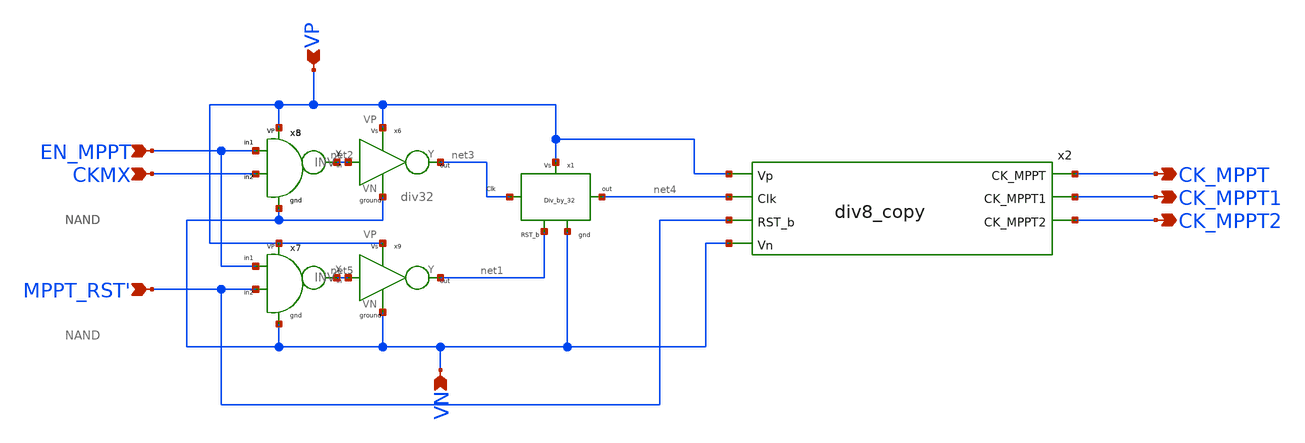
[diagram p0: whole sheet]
** sch_path: Blocks/MPPT/MPPT Clock initial stage.sch
**.subckt MPPT Clock initial stage CKMX MPPT_RST' VP EN_MPPT CK_MPPT CK_MPPT1 CK_MPPT2 VN
*.ipin CKMX
*.ipin MPPT_RST'
*.ipin VP
*.ipin EN_MPPT
*.opin CK_MPPT
*.opin CK_MPPT1
*.opin CK_MPPT2
*.ipin VN
x2 VP net4 CK_MPPT MPPT_RST' VN CK_MPPT1 CK_MPPT2 div8_copy
x1 net3 net4 VP VN net1 div32
x5 CKMX EN_MPPT net2 VP VN NAND
x7 MPPT_RST' EN_MPPT net5 VP VN NAND
x6 net2 net3 VP VN INV
x8 CKMX EN_MPPT net2 VP VN NAND
x9 net5 net1 VP VN INV
**.ends

* expanding   symbol:  Blocks/MPPT/div8_copy.sym # of pins=7
** sym_path: Blocks/MPPT/div8_copy.sym
** sch_path: Blocks/MPPT/div8_copy.sch
.subckt div8_copy Vp Clk CK_MPPT RST_b Vn CK_MPPT1 CK_MPPT2
*.ipin Clk
*.ipin RST_b
*.opin CK_MPPT
*.opin CK_MPPT1
*.opin CK_MPPT2
*.ipin Vn
*.ipin Vp
x1 net2 Clk RST_b Vn Vp net1 net2 DFF1
x2 net3 net1 RST_b Vn Vp net4 net3 DFF1
x3 net6 net4 RST_b Vn Vp net5 net6 DFF1
x4 net7 CK_MPPT Vp Vn INV
x5 net8 CK_MPPT1 Vp Vn INV
x7 net9 CK_MPPT2 Vp Vn INV
x8 net1 net12 Vp Vn INV
x11 net4 net11 Vp Vn INV
x12 net4 net10 Vp Vn INV
x6 net5 net11 net12 Vp Vn net9 NAND3
x9 net5 net10 net1 Vp Vn net8 NAND3
x10 net5 net4 net1 Vp Vn net7 NAND3
.ends


* expanding   symbol:  Blocks/Divide by 32 ckt/div32.sym # of pins=5
** sym_path: Blocks/Divide by 32 ckt/div32.sym
** sch_path: Blocks/Divide by 32 ckt/div32.sch
.subckt div32 Clk Clk/32 VP VN RST_b
*.opin Clk/32
*.ipin Clk
*.iopin VP
*.iopin VN
*.ipin RST_b
x1 net2 Clk RST_b VN VP net1 net2 DFF1
x6 net9 net10 VN VP Buff
x2 net3 net1 RST_b VN VP net4 net3 DFF1
x3 net8 net4 RST_b VN VP net5 net8 DFF1
x4 net7 net5 RST_b VN VP net6 net7 DFF1
x5 net9 net6 RST_b VN VP Clk/32 net10 DFF1
.ends


* expanding   symbol:  component/NAND2/NAND.sym # of pins=5
** sym_path: component/NAND2/NAND.sym
** sch_path: component/NAND2/NAND.sch
.subckt NAND B A Y VP VN
*.iopin VP
*.ipin A
*.ipin B
*.opin Y
*.iopin VN
XM1 Y A VP VP sky130_fd_pr__pfet_01v8 L=0.15 W=1.26 nf=1 ad='int((nf+1)/2) * W/nf * 0.29' as='int((nf+2)/2) * W/nf * 0.29'
+ pd='2*int((nf+1)/2) * (W/nf + 0.29)' ps='2*int((nf+2)/2) * (W/nf + 0.29)' nrd='0.29 / W' nrs='0.29 / W'
+ sa=0 sb=0 sd=0 mult=1 m=1
XM2 Y B VP VP sky130_fd_pr__pfet_01v8 L=0.15 W=1.26 nf=1 ad='int((nf+1)/2) * W/nf * 0.29' as='int((nf+2)/2) * W/nf * 0.29'
+ pd='2*int((nf+1)/2) * (W/nf + 0.29)' ps='2*int((nf+2)/2) * (W/nf + 0.29)' nrd='0.29 / W' nrs='0.29 / W'
+ sa=0 sb=0 sd=0 mult=1 m=1
XM3 Y A net1 net1 sky130_fd_pr__nfet_01v8 L=0.15 W=0.84 nf=1 ad='int((nf+1)/2) * W/nf * 0.29' as='int((nf+2)/2) * W/nf * 0.29'
+ pd='2*int((nf+1)/2) * (W/nf + 0.29)' ps='2*int((nf+2)/2) * (W/nf + 0.29)' nrd='0.29 / W' nrs='0.29 / W'
+ sa=0 sb=0 sd=0 mult=1 m=1
XM4 net1 B VN VN sky130_fd_pr__nfet_01v8 L=0.15 W=0.84 nf=1 ad='int((nf+1)/2) * W/nf * 0.29' as='int((nf+2)/2) * W/nf * 0.29'
+ pd='2*int((nf+1)/2) * (W/nf + 0.29)' ps='2*int((nf+2)/2) * (W/nf + 0.29)' nrd='0.29 / W' nrs='0.29 / W'
+ sa=0 sb=0 sd=0 mult=1 m=1
.ends


* expanding   symbol:  component/INV/INV.sym # of pins=4
** sym_path: component/INV/INV.sym
** sch_path: component/INV/INV.sch
.subckt INV X Y VP VN
*.ipin X
*.opin Y
*.iopin VN
*.iopin VP
XM1 Y X VN VN sky130_fd_pr__nfet_01v8 L=0.15 W=0.42 nf=1 ad='int((nf+1)/2) * W/nf * 0.29' as='int((nf+2)/2) * W/nf * 0.29'
+ pd='2*int((nf+1)/2) * (W/nf + 0.29)' ps='2*int((nf+2)/2) * (W/nf + 0.29)' nrd='0.29 / W' nrs='0.29 / W'
+ sa=0 sb=0 sd=0 mult=1 m=1
XM2 Y X VP VP sky130_fd_pr__pfet_01v8 L=0.15 W=1.26 nf=1 ad='int((nf+1)/2) * W/nf * 0.29' as='int((nf+2)/2) * W/nf * 0.29'
+ pd='2*int((nf+1)/2) * (W/nf + 0.29)' ps='2*int((nf+2)/2) * (W/nf + 0.29)' nrd='0.29 / W' nrs='0.29 / W'
+ sa=0 sb=0 sd=0 mult=1 m=1
.ends


* expanding   symbol:  component/FlipFlops/DFF1.sym # of pins=7
** sym_path: component/FlipFlops/DFF1.sym
** sch_path: component/FlipFlops/DFF1.sch
.subckt DFF1 D Clk RST VN VP Q Qb
*.opin Q
*.iopin VN
*.iopin VP
*.ipin Clk
*.ipin D
*.ipin RST
*.opin Qb
x7 net2 net4 net3 VP VN NAND
x8 net3 Clk RST VP VN net2 NAND3
x6 Q net1 RST VP VN Qb NAND3
x4 net2 Clk net4 VP VN net1 NAND3
x5 net1 D RST VP VN net4 NAND3
x1 Qb net2 Q VP VN NAND
.ends


* expanding   symbol:  component/NAND3/NAND3.sym # of pins=6
** sym_path: component/NAND3/NAND3.sym
** sch_path: component/NAND3/NAND3.sch
.subckt NAND3 A B C VP VN Y
*.iopin VP
*.iopin VN
*.ipin A
*.ipin B
*.ipin C
*.opin Y
XM1 Y A net1 VN sky130_fd_pr__nfet_01v8 L=0.15 W=1.26 nf=1 ad='int((nf+1)/2) * W/nf * 0.29' as='int((nf+2)/2) * W/nf * 0.29'
+ pd='2*int((nf+1)/2) * (W/nf + 0.29)' ps='2*int((nf+2)/2) * (W/nf + 0.29)' nrd='0.29 / W' nrs='0.29 / W'
+ sa=0 sb=0 sd=0 mult=1 m=1
XM2 net1 B net2 VN sky130_fd_pr__nfet_01v8 L=0.15 W=1.26 nf=1 ad='int((nf+1)/2) * W/nf * 0.29' as='int((nf+2)/2) * W/nf * 0.29'
+ pd='2*int((nf+1)/2) * (W/nf + 0.29)' ps='2*int((nf+2)/2) * (W/nf + 0.29)' nrd='0.29 / W' nrs='0.29 / W'
+ sa=0 sb=0 sd=0 mult=1 m=1
XM3 net2 C VN VN sky130_fd_pr__nfet_01v8 L=0.15 W=1.26 nf=1 ad='int((nf+1)/2) * W/nf * 0.29' as='int((nf+2)/2) * W/nf * 0.29'
+ pd='2*int((nf+1)/2) * (W/nf + 0.29)' ps='2*int((nf+2)/2) * (W/nf + 0.29)' nrd='0.29 / W' nrs='0.29 / W'
+ sa=0 sb=0 sd=0 mult=1 m=1
XM4 Y A VP VP sky130_fd_pr__pfet_01v8 L=0.15 W=1.26 nf=1 ad='int((nf+1)/2) * W/nf * 0.29' as='int((nf+2)/2) * W/nf * 0.29'
+ pd='2*int((nf+1)/2) * (W/nf + 0.29)' ps='2*int((nf+2)/2) * (W/nf + 0.29)' nrd='0.29 / W' nrs='0.29 / W'
+ sa=0 sb=0 sd=0 mult=1 m=1
XM5 Y B VP VP sky130_fd_pr__pfet_01v8 L=0.15 W=1.26 nf=1 ad='int((nf+1)/2) * W/nf * 0.29' as='int((nf+2)/2) * W/nf * 0.29'
+ pd='2*int((nf+1)/2) * (W/nf + 0.29)' ps='2*int((nf+2)/2) * (W/nf + 0.29)' nrd='0.29 / W' nrs='0.29 / W'
+ sa=0 sb=0 sd=0 mult=1 m=1
XM6 Y C VP VP sky130_fd_pr__pfet_01v8 L=0.15 W=1.26 nf=1 ad='int((nf+1)/2) * W/nf * 0.29' as='int((nf+2)/2) * W/nf * 0.29'
+ pd='2*int((nf+1)/2) * (W/nf + 0.29)' ps='2*int((nf+2)/2) * (W/nf + 0.29)' nrd='0.29 / W' nrs='0.29 / W'
+ sa=0 sb=0 sd=0 mult=1 m=1
.ends


* expanding   symbol:  Blocks/Buffer/Buff.sym # of pins=4
** sym_path: Blocks/Buffer/Buff.sym
** sch_path: Blocks/Buffer/Buff.sch
.subckt Buff X Y VP VN
*.ipin X
*.opin Y
*.iopin VN
*.iopin VP
x1 X net1 VP VN INV
x2 net1 Y VP VN INV
.ends

.end
